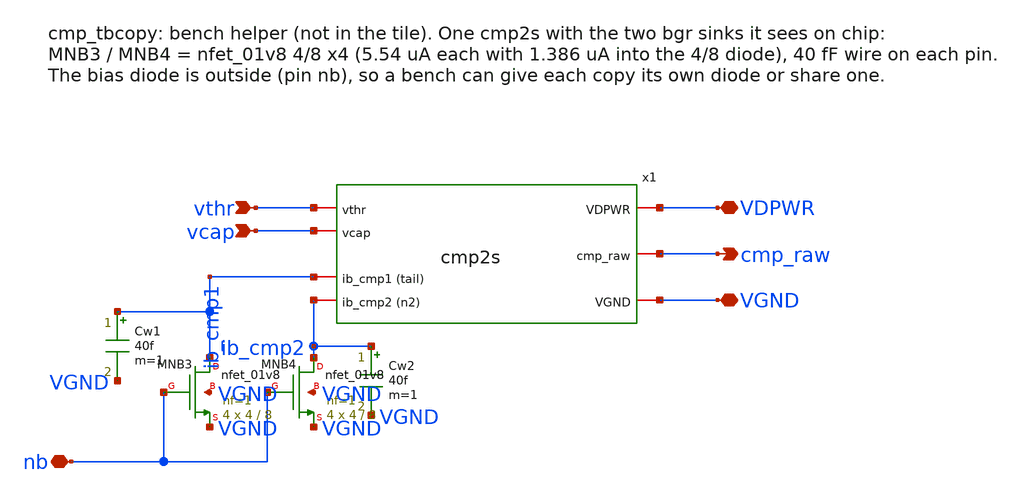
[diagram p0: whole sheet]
** sch_path: xschem/cmp_tbcopy.sch
**.subckt cmp_tbcopy vthr vcap nb VDPWR cmp_raw VGND
*.ipin vthr
*.ipin vcap
*.iopin nb
*.iopin VDPWR
*.opin cmp_raw
*.iopin VGND
x1 vthr vcap ib_cmp1 ib_cmp2 VDPWR cmp_raw VGND cmp2s
XMNB3 ib_cmp1 nb VGND VGND sky130_fd_pr__nfet_01v8 L=8 W=4 nf=1 ad='int((1 + 1)/2) * 4 / 1 * 0.29' as='int((1 + 2)/2) * 4 / 1 * 0.29'
+ pd='2*int((1 + 1)/2) * (4 / 1 + 0.29)' ps='2*int((1 + 2)/2) * (4 / 1 + 0.29)' nrd='0.29 / 4 ' nrs='0.29 / 4 '
+ sa=0 sb=0 sd=0 mult=4 m=4
XMNB4 ib_cmp2 nb VGND VGND sky130_fd_pr__nfet_01v8 L=8 W=4 nf=1 ad='int((1 + 1)/2) * 4 / 1 * 0.29' as='int((1 + 2)/2) * 4 / 1 * 0.29'
+ pd='2*int((1 + 1)/2) * (4 / 1 + 0.29)' ps='2*int((1 + 2)/2) * (4 / 1 + 0.29)' nrd='0.29 / 4 ' nrs='0.29 / 4 '
+ sa=0 sb=0 sd=0 mult=4 m=4
Cw1 ib_cmp1 VGND 40f m=1
Cw2 ib_cmp2 VGND 40f m=1
**.ends

* expanding   symbol:  cmp2s.sym # of pins=7
** sym_path: xschem/cmp2s.sym
** sch_path: xschem/cmp2s.sch
.subckt cmp2s vthr vcap ib_cmp1 ib_cmp2 VDPWR cmp_raw VGND
*.iopin VDPWR
*.iopin VGND
*.ipin vthr
*.ipin vcap
*.iopin ib_cmp1
*.iopin ib_cmp2
*.opin cmp_raw
XM2a nd nd VDPWR VDPWR sky130_fd_pr__pfet_01v8_lvt L=4 W=4 nf=1 ad='int((1 + 1)/2) * 4 / 1 * 0.29' as='int((1 + 2)/2) * 4 / 1 * 0.29'
+ pd='2*int((1 + 1)/2) * (4 / 1 + 0.29)' ps='2*int((1 + 2)/2) * (4 / 1 + 0.29)' nrd='0.29 / 4 ' nrs='0.29 / 4 '
+ sa=0 sb=0 sd=0 mult=8 m=8
XM2b n1 nd VDPWR VDPWR sky130_fd_pr__pfet_01v8_lvt L=4 W=4 nf=1 ad='int((1 + 1)/2) * 4 / 1 * 0.29' as='int((1 + 2)/2) * 4 / 1 * 0.29'
+ pd='2*int((1 + 1)/2) * (4 / 1 + 0.29)' ps='2*int((1 + 2)/2) * (4 / 1 + 0.29)' nrd='0.29 / 4 ' nrs='0.29 / 4 '
+ sa=0 sb=0 sd=0 mult=8 m=8
XM1a nd vthr ib_cmp1 VGND sky130_fd_pr__nfet_01v8_lvt L=1.75 W=10 nf=1 ad='int((1 + 1)/2) * 10 / 1 * 0.29'
+ as='int((1 + 2)/2) * 10 / 1 * 0.29' pd='2*int((1 + 1)/2) * (10 / 1 + 0.29)' ps='2*int((1 + 2)/2) * (10 / 1 + 0.29)'
+ nrd='0.29 / 10 ' nrs='0.29 / 10 ' sa=0 sb=0 sd=0 mult=6 m=6
XM1b n1 vcap ib_cmp1 VGND sky130_fd_pr__nfet_01v8_lvt L=1.75 W=10 nf=1 ad='int((1 + 1)/2) * 10 / 1 * 0.29'
+ as='int((1 + 2)/2) * 10 / 1 * 0.29' pd='2*int((1 + 1)/2) * (10 / 1 + 0.29)' ps='2*int((1 + 2)/2) * (10 / 1 + 0.29)'
+ nrd='0.29 / 10 ' nrs='0.29 / 10 ' sa=0 sb=0 sd=0 mult=6 m=6
XM3 ib_cmp2 n1 VDPWR VDPWR sky130_fd_pr__pfet_01v8_lvt L=1 W=4 nf=1 ad='int((1 + 1)/2) * 4 / 1 * 0.29'
+ as='int((1 + 2)/2) * 4 / 1 * 0.29' pd='2*int((1 + 1)/2) * (4 / 1 + 0.29)' ps='2*int((1 + 2)/2) * (4 / 1 + 0.29)'
+ nrd='0.29 / 4 ' nrs='0.29 / 4 ' sa=0 sb=0 sd=0 mult=3 m=3
XMIP x ib_cmp2 VDPWR VDPWR sky130_fd_pr__pfet_01v8 L=1 W=0.42 nf=1 ad='int((1 + 1)/2) * 0.42 / 1 * 0.29'
+ as='int((1 + 2)/2) * 0.42 / 1 * 0.29' pd='2*int((1 + 1)/2) * (0.42 / 1 + 0.29)' ps='2*int((1 + 2)/2) * (0.42 / 1 + 0.29)'
+ nrd='0.29 / 0.42 ' nrs='0.29 / 0.42 ' sa=0 sb=0 sd=0 mult=1 m=1
XMIN x ib_cmp2 VGND VGND sky130_fd_pr__nfet_01v8 L=0.15 W=2 nf=1 ad='int((1 + 1)/2) * 2 / 1 * 0.29' as='int((1 + 2)/2) * 2 / 1 * 0.29'
+ pd='2*int((1 + 1)/2) * (2 / 1 + 0.29)' ps='2*int((1 + 2)/2) * (2 / 1 + 0.29)' nrd='0.29 / 2 ' nrs='0.29 / 2 '
+ sa=0 sb=0 sd=0 mult=1 m=1
xinv x VGND VGND VDPWR VDPWR cmp_raw sky130_fd_sc_hd__inv_1
.ends

.end
